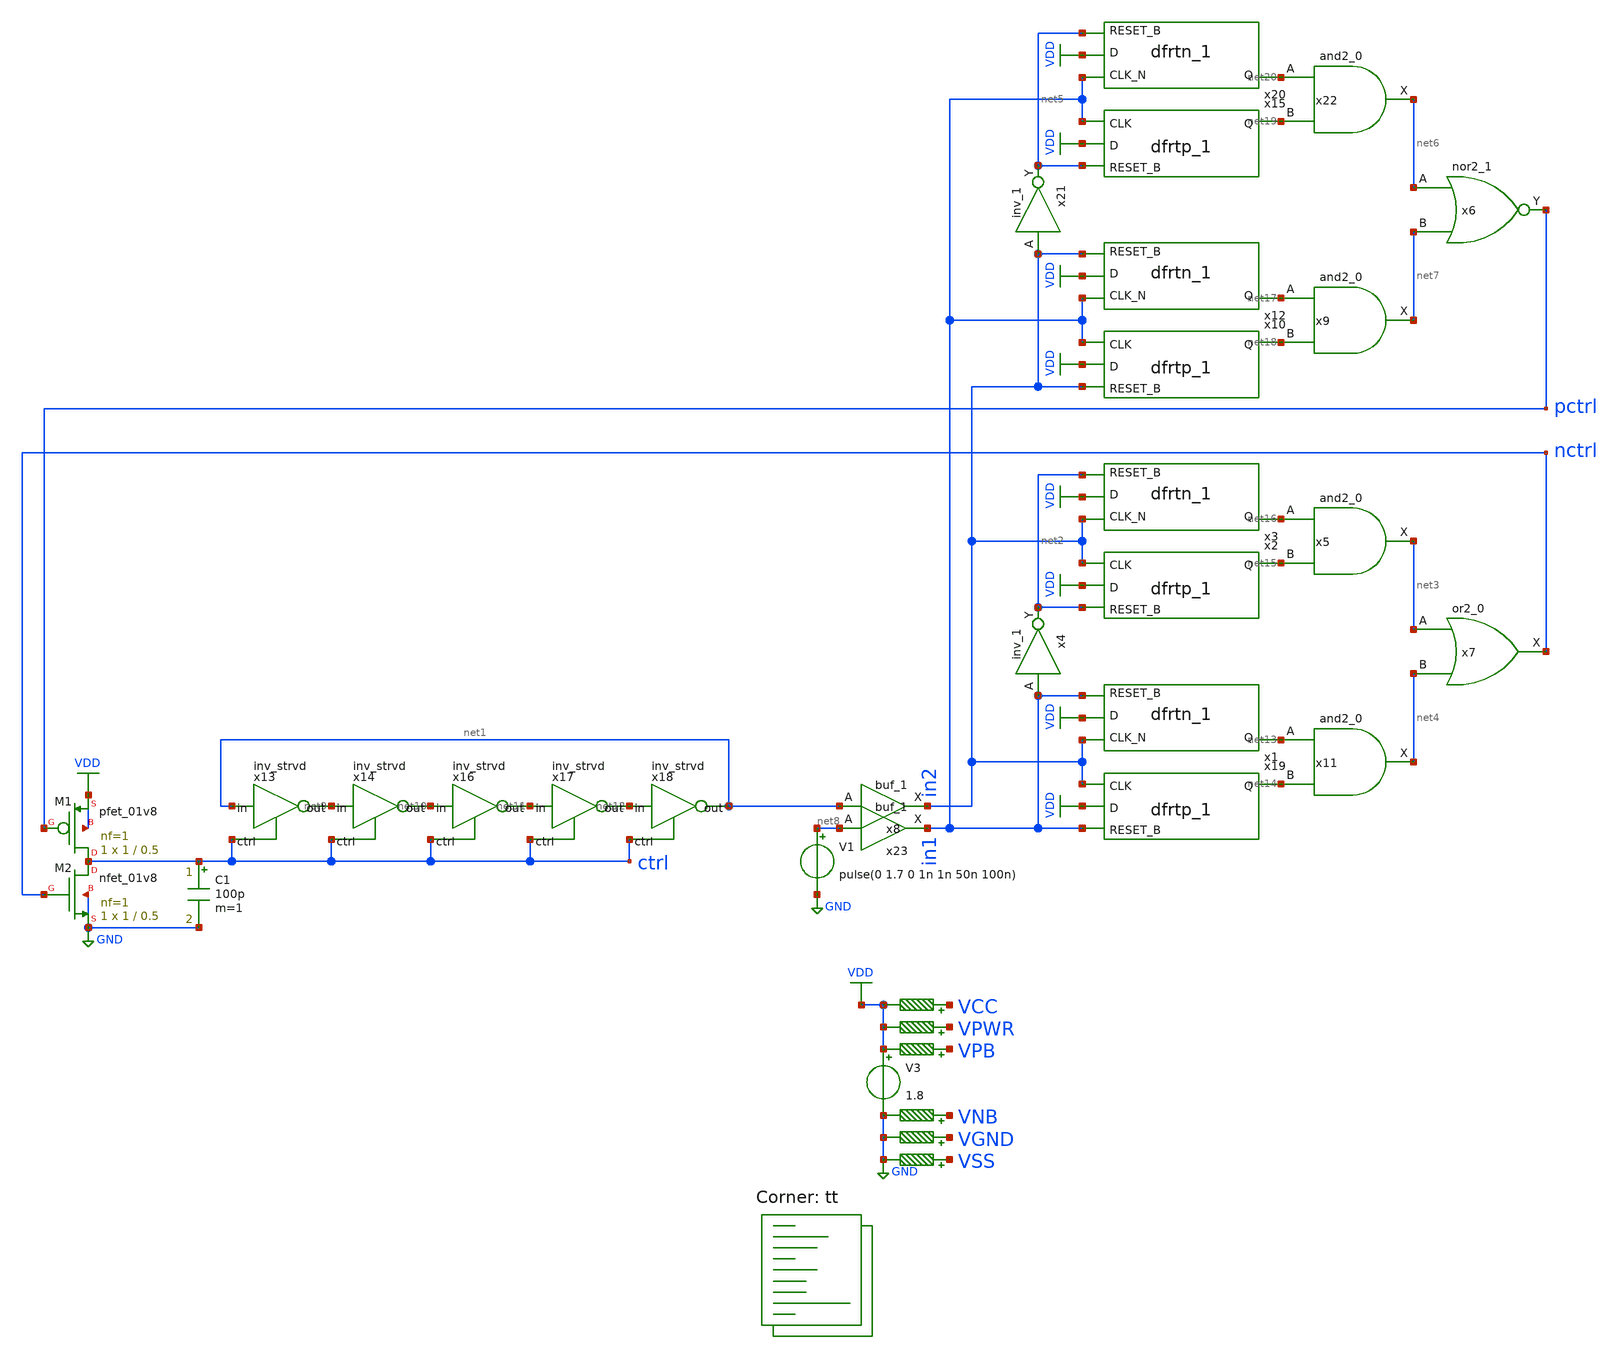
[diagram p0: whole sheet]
** sch_path: freq_det.sch
**.subckt freq_det
V3 VDD GND 1.8
R1 VNB GND 0.01 m=1
R2 VPB VDD 0.01 m=1
R3 VPWR VDD 0.01 m=1
R4 VGND GND 0.01 m=1
R5 VSS GND 0.01 m=1
R6 VCC VDD 0.01 m=1
V1 net8 GND pulse(0 1.7 0 1n 1n 50n 100n)
x13 net1 net9 ctrl VDD GND inv_strvd
x14 net9 net10 ctrl VDD GND inv_strvd
x16 net10 net11 ctrl VDD GND inv_strvd
x17 net11 net12 ctrl VDD GND inv_strvd
x18 net12 net1 ctrl VDD GND inv_strvd
XM1 ctrl pctrl VDD VDD sky130_fd_pr__pfet_01v8 L=0.5 W=1 nf=1 ad='int((nf+1)/2) * W/nf * 0.29' as='int((nf+2)/2) * W/nf * 0.29'
+ pd='2*int((nf+1)/2) * (W/nf + 0.29)' ps='2*int((nf+2)/2) * (W/nf + 0.29)' nrd='0.29 / W' nrs='0.29 / W'
+ sa=0 sb=0 sd=0 mult=1 m=1
XM2 ctrl nctrl GND GND sky130_fd_pr__nfet_01v8 L=0.5 W=1 nf=1 ad='int((nf+1)/2) * W/nf * 0.29' as='int((nf+2)/2) * W/nf * 0.29'
+ pd='2*int((nf+1)/2) * (W/nf + 0.29)' ps='2*int((nf+2)/2) * (W/nf + 0.29)' nrd='0.29 / W' nrs='0.29 / W'
+ sa=0 sb=0 sd=0 mult=1 m=1
C1 ctrl GND 100p m=1
x8 net1 VGND VNB VPB VPWR in2 sky130_fd_sc_hd__buf_1
x7 net3 net4 VGND VNB VPB VPWR nctrl sky130_fd_sc_hd__or2_0
x11 net13 net14 VGND VNB VPB VPWR net4 sky130_fd_sc_hd__and2_0
x19 in2 VDD in1 VGND VNB VPB VPWR net14 sky130_fd_sc_hd__dfrtp_1
x1 in2 VDD in1 VGND VNB VPB VPWR net13 sky130_fd_sc_hd__dfrtn_1
x2 in2 VDD net2 VGND VNB VPB VPWR net15 sky130_fd_sc_hd__dfrtp_1
x3 in2 VDD net2 VGND VNB VPB VPWR net16 sky130_fd_sc_hd__dfrtn_1
x4 in1 VGND VNB VPB VPWR net2 sky130_fd_sc_hd__inv_1
x5 net16 net15 VGND VNB VPB VPWR net3 sky130_fd_sc_hd__and2_0
x9 net17 net18 VGND VNB VPB VPWR net7 sky130_fd_sc_hd__and2_0
x10 in1 VDD in2 VGND VNB VPB VPWR net18 sky130_fd_sc_hd__dfrtp_1
x12 in1 VDD in2 VGND VNB VPB VPWR net17 sky130_fd_sc_hd__dfrtn_1
x15 in1 VDD net5 VGND VNB VPB VPWR net19 sky130_fd_sc_hd__dfrtp_1
x20 in1 VDD net5 VGND VNB VPB VPWR net20 sky130_fd_sc_hd__dfrtn_1
x21 in2 VGND VNB VPB VPWR net5 sky130_fd_sc_hd__inv_1
x22 net20 net19 VGND VNB VPB VPWR net6 sky130_fd_sc_hd__and2_0
x6 net6 net7 VGND VNB VPB VPWR pctrl sky130_fd_sc_hd__nor2_1
x23 net8 VGND VNB VPB VPWR in1 sky130_fd_sc_hd__buf_1
**** begin user architecture code
.lib $::SKYWATER_MODELS/sky130.lib.spice tt


.include /usr/local/share/pdk/sky130A/libs.ref/sky130_fd_sc_hd/spice/sky130_fd_sc_hd.spice tt
.control
  save all
  tran .1n 250m
  write top.raw
  quit 0
.endc


**** end user architecture code
**.ends

* expanding   symbol:  tt_um_wulf_8bit_vco/xschem/lib/inv_strvd.sym # of pins=3
** sym_path: archive/tt_um_wulf_8bit_vco/xschem/lib/inv_strvd.sym
** sch_path: archive/tt_um_wulf_8bit_vco/xschem/lib/inv_strvd.sch
.subckt inv_strvd in out ctrl VDD VSS
*.ipin in
*.ipin ctrl
*.opin out
XM2 out in net1 net1 sky130_fd_pr__nfet_01v8 L=1 W=40 nf=1 ad='int((1 + 1)/2) * 40 / 1 * 0.29' as='int((1 + 2)/2) * 40 / 1 * 0.29'
+ pd='2*int((1 + 1)/2) * (40 / 1 + 0.29)' ps='2*int((1 + 2)/2) * (40 / 1 + 0.29)' nrd='0.29 / 40 ' nrs='0.29 / 40 '
+ sa=0 sb=0 sd=0 mult=1 m=1
XM3 net1 ctrl VSS VSS sky130_fd_pr__nfet_01v8 L=0.15 W=1 nf=1 ad='int((1 + 1)/2) * 1 / 1 * 0.29' as='int((1 + 2)/2) * 1 / 1 * 0.29'
+ pd='2*int((1 + 1)/2) * (1 / 1 + 0.29)' ps='2*int((1 + 2)/2) * (1 / 1 + 0.29)' nrd='0.29 / 1 ' nrs='0.29 / 1 '
+ sa=0 sb=0 sd=0 mult=1 m=1
XM1 out in VDD VDD sky130_fd_pr__pfet_01v8 L=4 W=40 nf=1 ad='int((nf+1)/2) * W/nf * 0.29' as='int((nf+2)/2) * W/nf * 0.29'
+ pd='2*int((nf+1)/2) * (W/nf + 0.29)' ps='2*int((nf+2)/2) * (W/nf + 0.29)' nrd='0.29 / W' nrs='0.29 / W'
+ sa=0 sb=0 sd=0 mult=1 m=1
.ends

.GLOBAL GND
.GLOBAL VDD
.end
